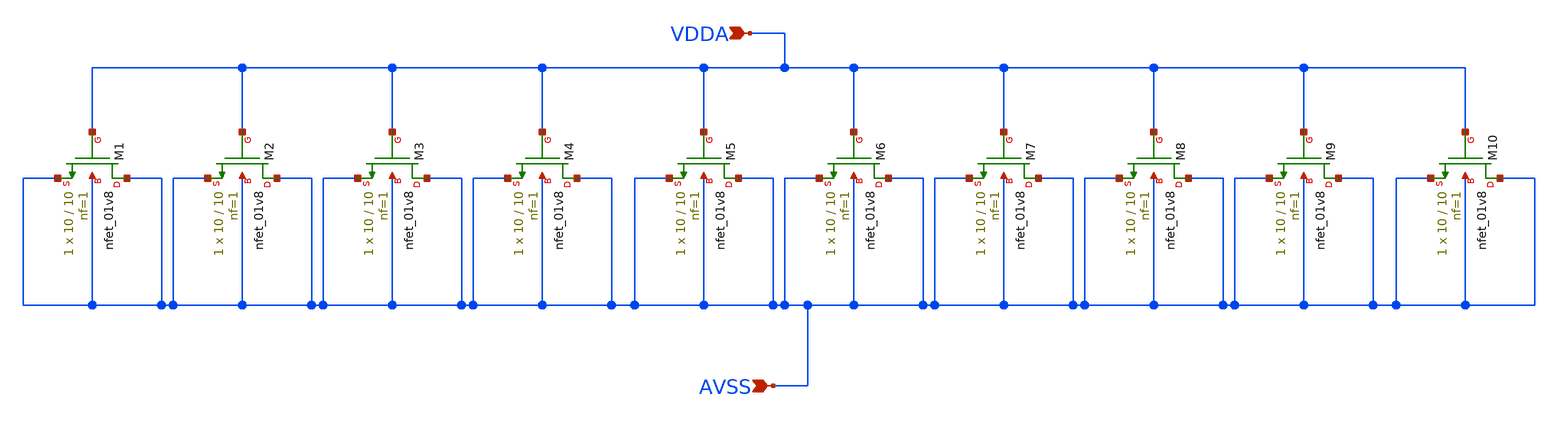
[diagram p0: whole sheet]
** sch_path: lef/lef/gds/bg2_moscap.sch
**.subckt bg2_moscap VDDA AVSS
*.ipin VDDA
*.ipin AVSS
XM1 AVSS VDDA AVSS AVSS sky130_fd_pr__nfet_01v8 L=10 W=10 nf=1 ad='int((1 + 1)/2) * 10 / 1 * 0.29' as='int((1 + 2)/2) * 10 / 1 * 0.29'
+ pd='2*int((1 + 1)/2) * (10 / 1 + 0.29)' ps='2*int((1 + 2)/2) * (10 / 1 + 0.29)' nrd='0.29 / 10 ' nrs='0.29 / 10 '
+ sa=0 sb=0 sd=0 mult=1 m=1
XM2 AVSS VDDA AVSS AVSS sky130_fd_pr__nfet_01v8 L=10 W=10 nf=1 ad='int((1 + 1)/2) * 10 / 1 * 0.29' as='int((1 + 2)/2) * 10 / 1 * 0.29'
+ pd='2*int((1 + 1)/2) * (10 / 1 + 0.29)' ps='2*int((1 + 2)/2) * (10 / 1 + 0.29)' nrd='0.29 / 10 ' nrs='0.29 / 10 '
+ sa=0 sb=0 sd=0 mult=1 m=1
XM3 AVSS VDDA AVSS AVSS sky130_fd_pr__nfet_01v8 L=10 W=10 nf=1 ad='int((1 + 1)/2) * 10 / 1 * 0.29' as='int((1 + 2)/2) * 10 / 1 * 0.29'
+ pd='2*int((1 + 1)/2) * (10 / 1 + 0.29)' ps='2*int((1 + 2)/2) * (10 / 1 + 0.29)' nrd='0.29 / 10 ' nrs='0.29 / 10 '
+ sa=0 sb=0 sd=0 mult=1 m=1
XM4 AVSS VDDA AVSS AVSS sky130_fd_pr__nfet_01v8 L=10 W=10 nf=1 ad='int((1 + 1)/2) * 10 / 1 * 0.29' as='int((1 + 2)/2) * 10 / 1 * 0.29'
+ pd='2*int((1 + 1)/2) * (10 / 1 + 0.29)' ps='2*int((1 + 2)/2) * (10 / 1 + 0.29)' nrd='0.29 / 10 ' nrs='0.29 / 10 '
+ sa=0 sb=0 sd=0 mult=1 m=1
XM5 AVSS VDDA AVSS AVSS sky130_fd_pr__nfet_01v8 L=10 W=10 nf=1 ad='int((1 + 1)/2) * 10 / 1 * 0.29' as='int((1 + 2)/2) * 10 / 1 * 0.29'
+ pd='2*int((1 + 1)/2) * (10 / 1 + 0.29)' ps='2*int((1 + 2)/2) * (10 / 1 + 0.29)' nrd='0.29 / 10 ' nrs='0.29 / 10 '
+ sa=0 sb=0 sd=0 mult=1 m=1
XM6 AVSS VDDA AVSS AVSS sky130_fd_pr__nfet_01v8 L=10 W=10 nf=1 ad='int((1 + 1)/2) * 10 / 1 * 0.29' as='int((1 + 2)/2) * 10 / 1 * 0.29'
+ pd='2*int((1 + 1)/2) * (10 / 1 + 0.29)' ps='2*int((1 + 2)/2) * (10 / 1 + 0.29)' nrd='0.29 / 10 ' nrs='0.29 / 10 '
+ sa=0 sb=0 sd=0 mult=1 m=1
XM7 AVSS VDDA AVSS AVSS sky130_fd_pr__nfet_01v8 L=10 W=10 nf=1 ad='int((1 + 1)/2) * 10 / 1 * 0.29' as='int((1 + 2)/2) * 10 / 1 * 0.29'
+ pd='2*int((1 + 1)/2) * (10 / 1 + 0.29)' ps='2*int((1 + 2)/2) * (10 / 1 + 0.29)' nrd='0.29 / 10 ' nrs='0.29 / 10 '
+ sa=0 sb=0 sd=0 mult=1 m=1
XM8 AVSS VDDA AVSS AVSS sky130_fd_pr__nfet_01v8 L=10 W=10 nf=1 ad='int((1 + 1)/2) * 10 / 1 * 0.29' as='int((1 + 2)/2) * 10 / 1 * 0.29'
+ pd='2*int((1 + 1)/2) * (10 / 1 + 0.29)' ps='2*int((1 + 2)/2) * (10 / 1 + 0.29)' nrd='0.29 / 10 ' nrs='0.29 / 10 '
+ sa=0 sb=0 sd=0 mult=1 m=1
XM9 AVSS VDDA AVSS AVSS sky130_fd_pr__nfet_01v8 L=10 W=10 nf=1 ad='int((1 + 1)/2) * 10 / 1 * 0.29' as='int((1 + 2)/2) * 10 / 1 * 0.29'
+ pd='2*int((1 + 1)/2) * (10 / 1 + 0.29)' ps='2*int((1 + 2)/2) * (10 / 1 + 0.29)' nrd='0.29 / 10 ' nrs='0.29 / 10 '
+ sa=0 sb=0 sd=0 mult=1 m=1
XM10 AVSS VDDA AVSS AVSS sky130_fd_pr__nfet_01v8 L=10 W=10 nf=1 ad='int((1 + 1)/2) * 10 / 1 * 0.29' as='int((1 + 2)/2) * 10 / 1 * 0.29'
+ pd='2*int((1 + 1)/2) * (10 / 1 + 0.29)' ps='2*int((1 + 2)/2) * (10 / 1 + 0.29)' nrd='0.29 / 10 ' nrs='0.29 / 10 '
+ sa=0 sb=0 sd=0 mult=1 m=1
**.ends
.end
